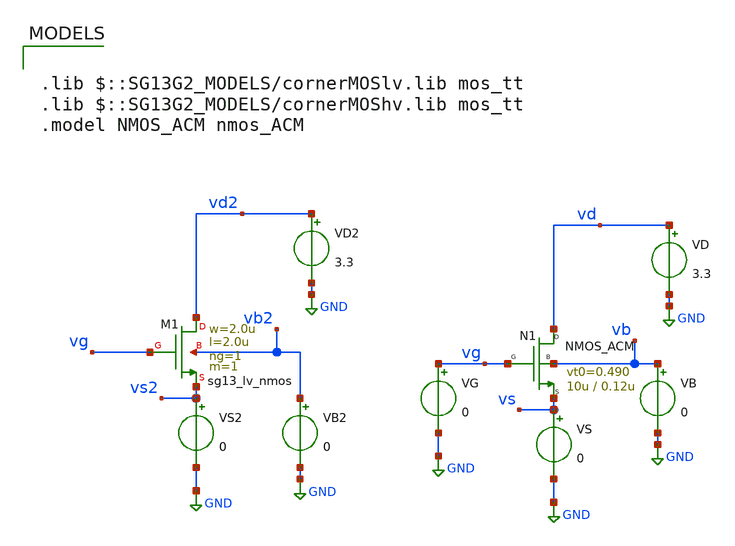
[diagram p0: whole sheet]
** sch_path: legacy/Examples/IHP-SG13/xschem/Extraction/TB_nmos_acm.sch
**.subckt TB_nmos_acm
VG vg GND 0
VD vd GND 3.3
VB vb GND 0
VS vs GND 0
VD2 vd2 GND 3.3
VB2 vb2 GND 0
VS2 vs2 GND 0
XM1 vd2 vg vs2 vb2 sg13_lv_nmos w=2.0u l=2.0u ng=1 m=1 mm_ok=1
N1 vd vg vs vb NMOS_ACM w=10u l=0.12u n=1.41 is=11.7u vt0=0.490 sigma=52.8m zeta=1p
**** begin user architecture code

.lib $::SG13G2_MODELS/cornerMOSlv.lib mos_tt
.lib $::SG13G2_MODELS/cornerMOShv.lib mos_tt
.model NMOS_ACM nmos_ACM



.control
pre_osdi /home/gmaranhao/Documents/MOSFET_model/Examples/GF180MCU/xschem/symbol/NMOS_ACM_2V0.osdi
save all

dc VG 0.1 3.3 5m

*gm for ACM
let gm_id = deriv(ln(i(Vs)))

*gm for GF180
let gm_id_gf = deriv(ln(i(Vs2)))

save gm_id gm_id_gf
write TB_nmos_acm.raw

.endc


**** end user architecture code
**.ends
.GLOBAL GND
.end
